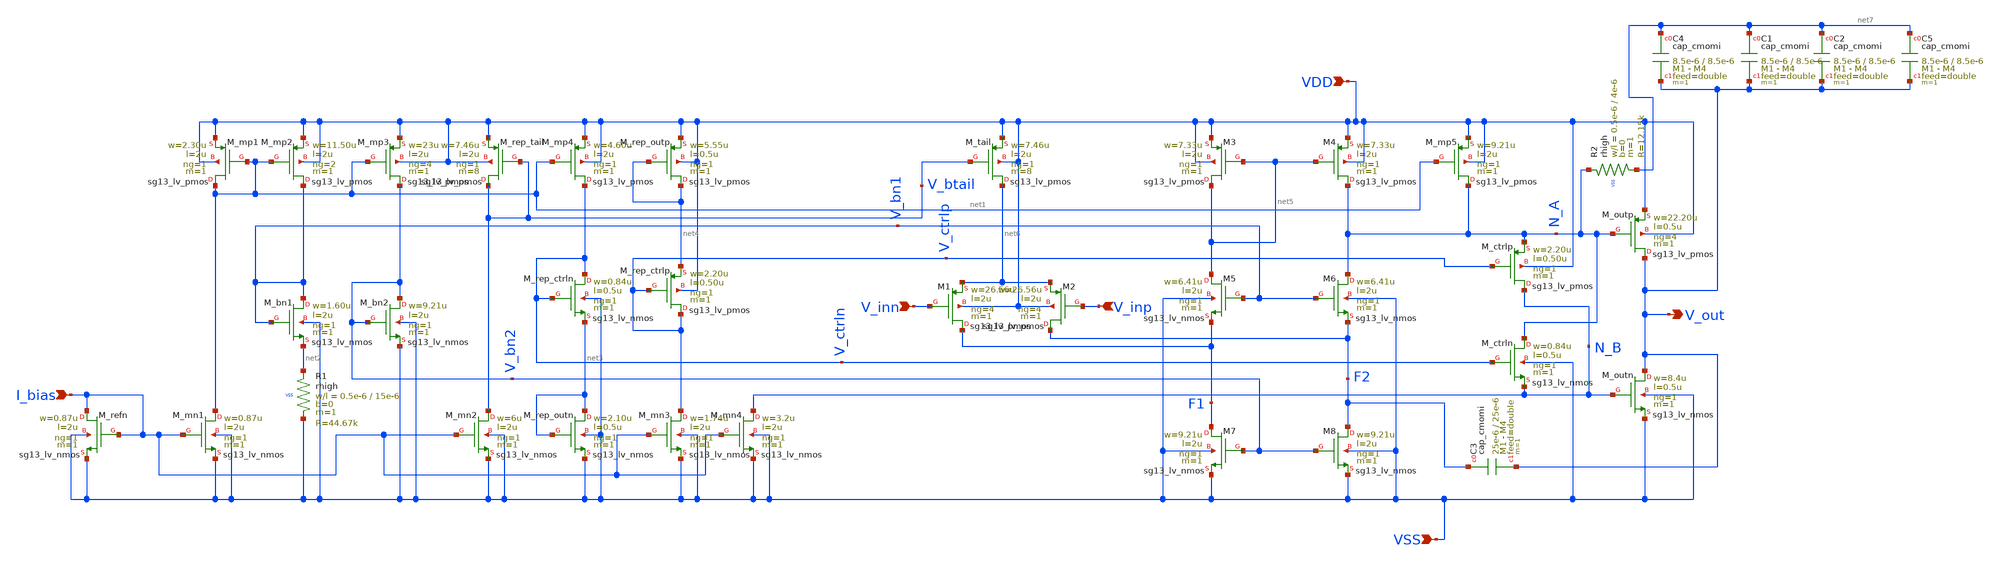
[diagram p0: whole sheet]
** sch_path: xschem/gain_stage/gain_ota.sch
**.subckt gain_ota V_inn VDD VSS V_out I_bias V_inp
*.ipin V_inn
*.ipin VDD
*.ipin VSS
*.opin V_out
*.ipin I_bias
*.ipin V_inp
XM1 F1 V_inn net6 VDD sg13_lv_pmos w=26.56u l=2u ng=4 m=1 mm_ok=1
XM2 F2 V_inp net6 VDD sg13_lv_pmos w=26.56u l=2u ng=4 m=1 mm_ok=1
XM3 net5 net5 VDD VDD sg13_lv_pmos w=7.33u l=2u ng=1 m=1 mm_ok=1
XM4 N_A net5 VDD VDD sg13_lv_pmos w=7.33u l=2u ng=1 m=1 mm_ok=1
XM7 F1 V_bn2 VSS VSS sg13_lv_nmos w=9.21u l=2u ng=1 m=1 mm_ok=1
XM8 F2 V_bn2 VSS VSS sg13_lv_nmos w=9.21u l=2u ng=1 m=1 mm_ok=1
XM_tail net6 V_btail VDD VDD sg13_lv_pmos w=7.46u l=2u ng=1 m=8 mm_ok=1
XM_ctrlp N_B V_ctrlp N_A VDD sg13_lv_pmos w=2.20u l=0.50u ng=1 m=1 mm_ok=1
XM_outp V_out N_A VDD VDD sg13_lv_pmos w=22.20u l=0.5u ng=4 m=1 mm_ok=1
XM_ctrln N_A V_ctrln N_B VSS sg13_lv_nmos w=0.84u l=0.5u ng=1 m=1 mm_ok=1
XM_outn V_out N_B VSS VSS sg13_lv_nmos w=8.4u l=0.5u ng=1 m=1 mm_ok=1
XM5 net5 V_bn1 F1 VSS sg13_lv_nmos w=6.41u l=2u ng=1 m=1 mm_ok=1
XM6 N_A V_bn1 F2 VSS sg13_lv_nmos w=6.41u l=2u ng=1 m=1 mm_ok=1
XM_mp1 net1 net1 VDD VDD sg13_lv_pmos w=2.30u l=2u ng=1 m=1 mm_ok=1
XM_mn1 net1 I_bias VSS VSS sg13_lv_nmos w=0.87u l=2u ng=1 m=1 mm_ok=1
XM_refn I_bias I_bias VSS VSS sg13_lv_nmos w=0.87u l=2u ng=1 m=1 mm_ok=1
XM_mp2 V_bn1 net1 VDD VDD sg13_lv_pmos w=11.50u l=2u ng=2 m=1 mm_ok=1
XM_mp3 V_bn2 net1 VDD VDD sg13_lv_pmos w=23u l=2u ng=4 m=1 mm_ok=1
XM_bn1 V_bn1 V_bn1 net2 VSS sg13_lv_nmos w=1.60u l=2u ng=1 m=1 mm_ok=1
XM_bn2 V_bn2 V_bn2 VSS VSS sg13_lv_nmos w=9.21u l=2u ng=1 m=1 mm_ok=1
XM_mn2 V_btail I_bias VSS VSS sg13_lv_nmos w=6u l=2u ng=1 m=1 mm_ok=1
XM_rep_tail V_btail V_btail VDD VDD sg13_lv_pmos w=7.46u l=2u ng=1 m=8 mm_ok=1
XM_mn4 N_B I_bias VSS VSS sg13_lv_nmos w=3.2u l=2u ng=1 m=1 mm_ok=1
XR1 net2 VSS VSS rhigh w=0.5e-6 l=15e-6 m=1 b=0 mm_ok=1
XM_mp4 V_ctrln net1 VDD VDD sg13_lv_pmos w=4.60u l=2u ng=1 m=1 mm_ok=1
XM_rep_ctrln V_ctrln V_ctrln net3 VSS sg13_lv_nmos w=0.84u l=0.5u ng=1 m=1 mm_ok=1
XM_rep_outn net3 net3 VSS VSS sg13_lv_nmos w=2.10u l=0.5u ng=1 m=1 mm_ok=1
XM_mn3 V_ctrlp I_bias VSS VSS sg13_lv_nmos w=1.74u l=2u ng=1 m=1 mm_ok=1
XM_rep_outp net4 net4 VDD VDD sg13_lv_pmos w=5.55u l=0.5u ng=1 m=1 mm_ok=1
XM_rep_ctrlp V_ctrlp V_ctrlp net4 VDD sg13_lv_pmos w=2.20u l=0.50u ng=1 m=1 mm_ok=1
XM_mp5 N_A net1 VDD VDD sg13_lv_pmos w=9.21u l=2u ng=1 m=1 mm_ok=1
XR2 N_A net7 VSS rhigh w=0.5e-6 l=4e-6 m=1 b=0 mm_ok=1
XC3 F2 V_out cap_cmomi w=25e-6 l=25e-6 mmin=1 mmax=4 feed=double subblock=0 m=1 mm_ok=1
XC4 net7 V_out cap_cmomi w=8.5e-6 l=8.5e-6 mmin=1 mmax=4 feed=double subblock=0 m=1 mm_ok=1
XC1 net7 V_out cap_cmomi w=8.5e-6 l=8.5e-6 mmin=1 mmax=4 feed=double subblock=0 m=1 mm_ok=1
XC2 net7 V_out cap_cmomi w=8.5e-6 l=8.5e-6 mmin=1 mmax=4 feed=double subblock=0 m=1 mm_ok=1
XC5 net7 V_out cap_cmomi w=8.5e-6 l=8.5e-6 mmin=1 mmax=4 feed=double subblock=0 m=1 mm_ok=1
**.ends
.end
